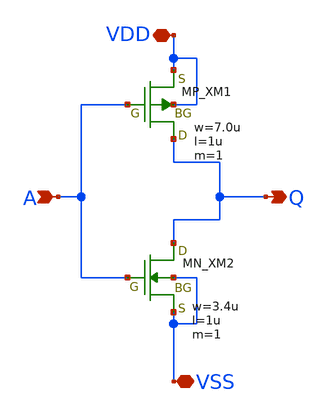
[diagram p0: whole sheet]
** sch_path: member_project/inverter_MUX/INV_06.sch
**.subckt INV_06 A Q VDD VSS
*.ipin A
*.opin Q
*.iopin VDD
*.iopin VSS
XM1 Q A VDD VDD PMOS w=7.0u l=1u as=0 ad=0 ps=0 pd=0 nrd=0 nrs=0 m=1
XM2 Q A VSS VSS NMOS w=3.4u l=1u as=0 ad=0 ps=0 pd=0 nrd=0 nrs=0 m=1
**.ends
.end
